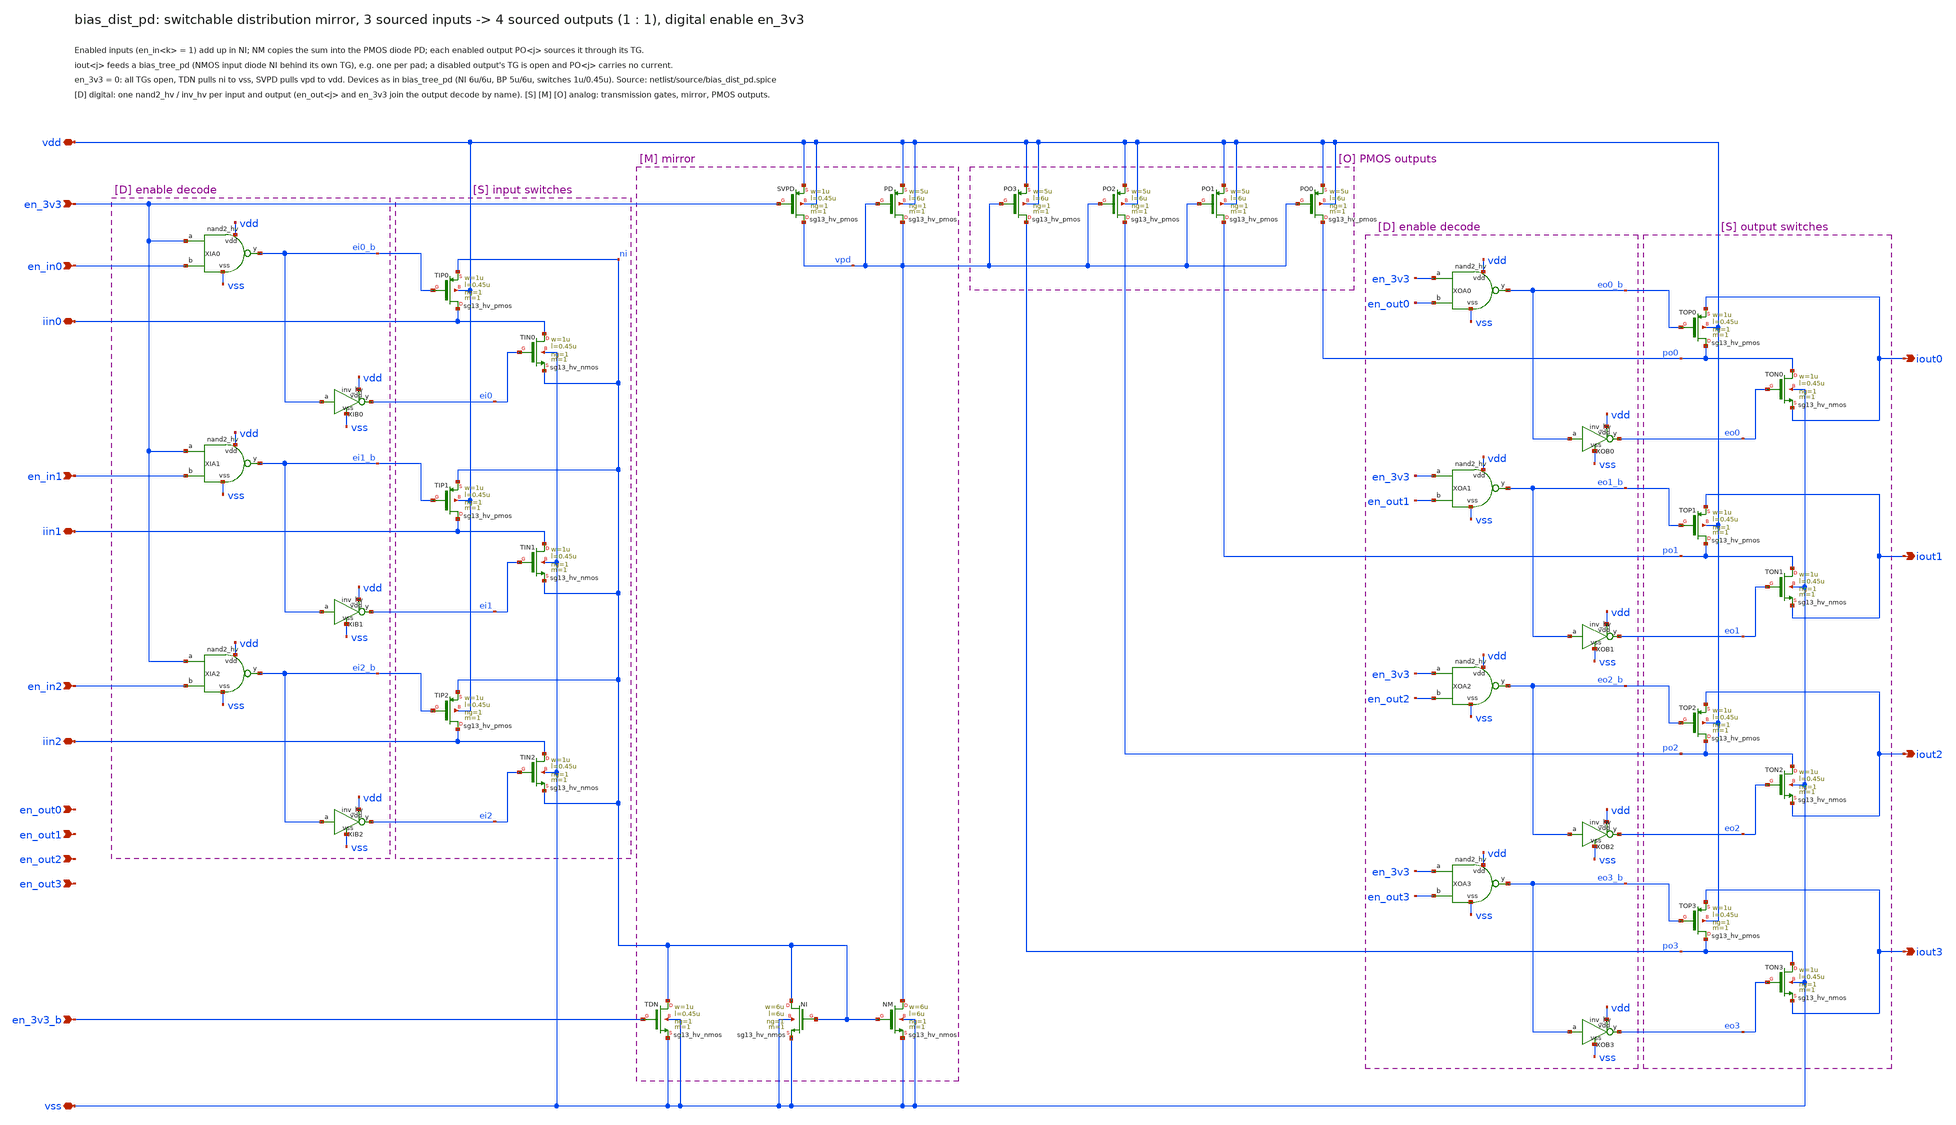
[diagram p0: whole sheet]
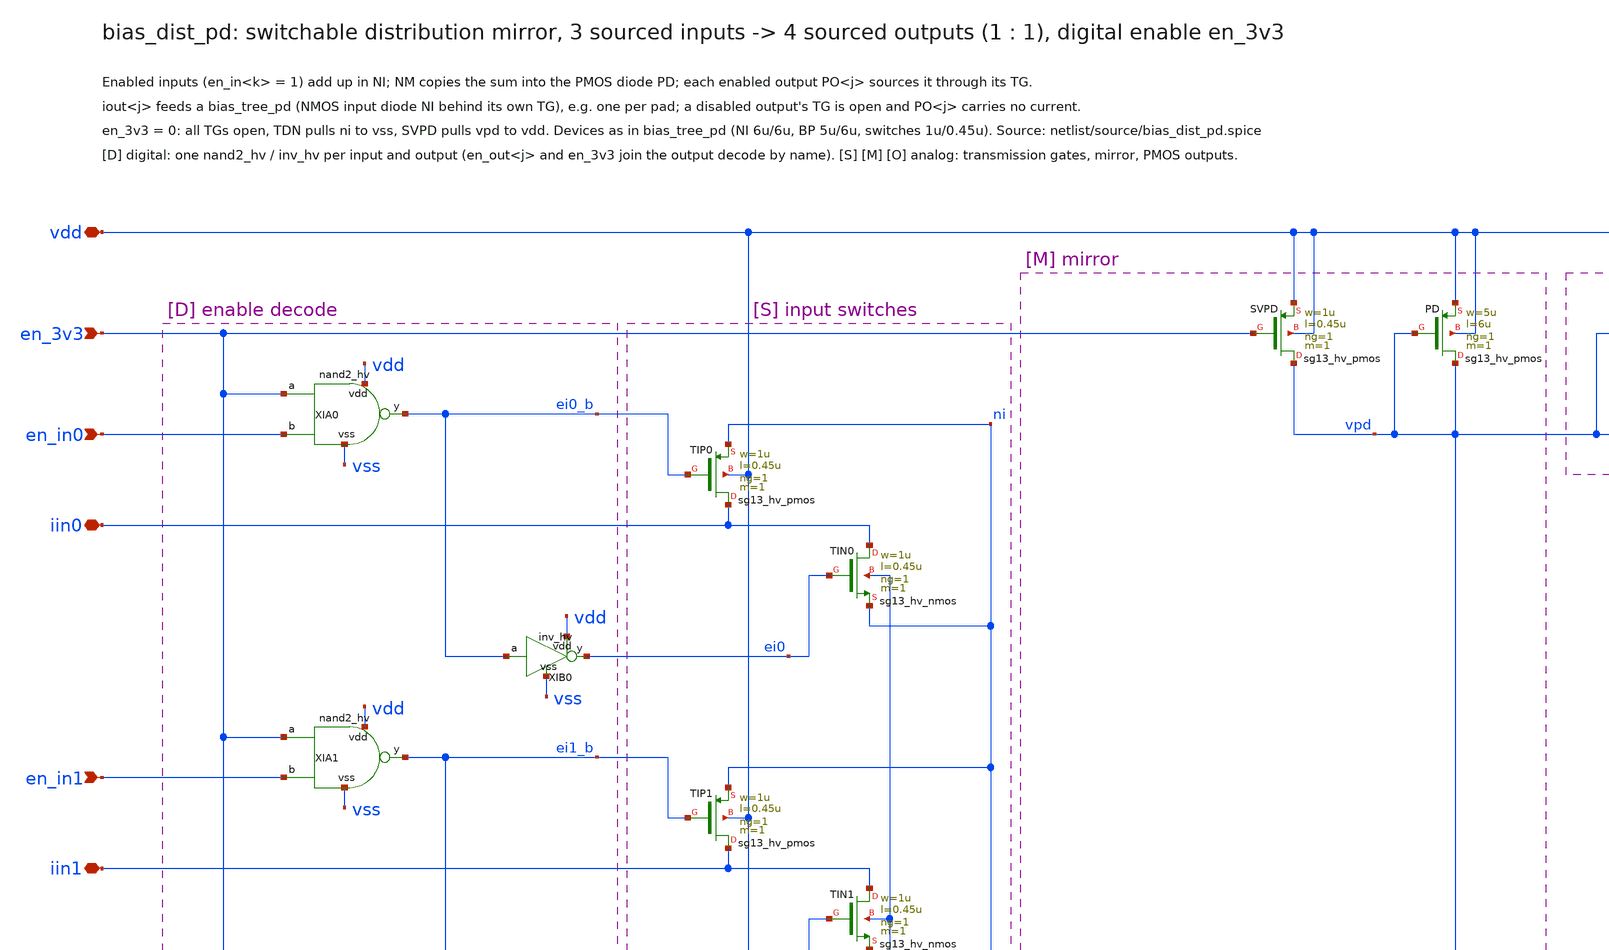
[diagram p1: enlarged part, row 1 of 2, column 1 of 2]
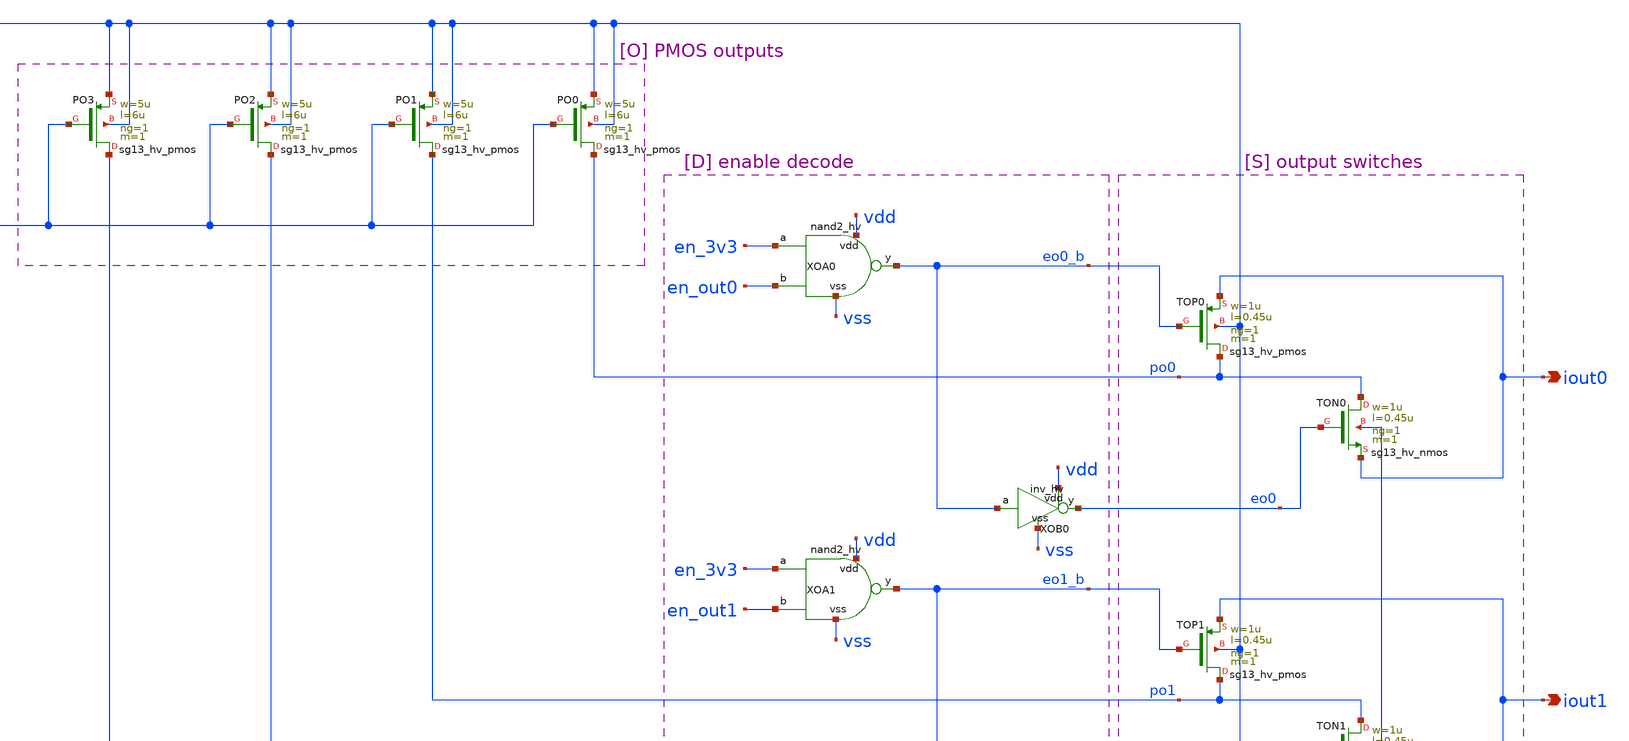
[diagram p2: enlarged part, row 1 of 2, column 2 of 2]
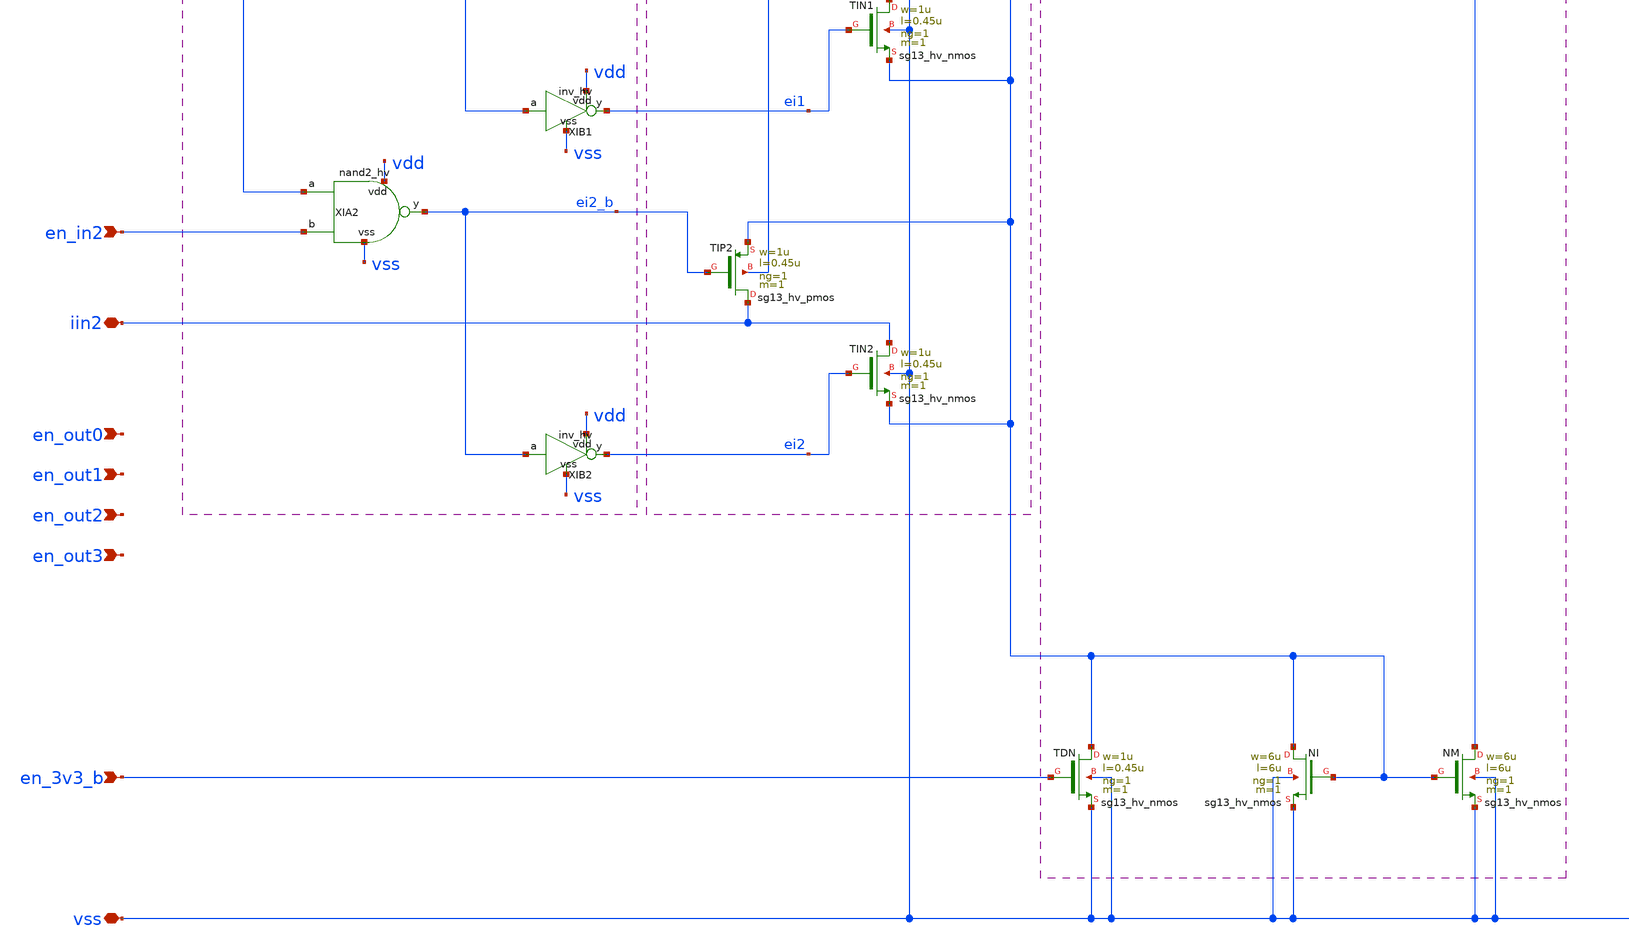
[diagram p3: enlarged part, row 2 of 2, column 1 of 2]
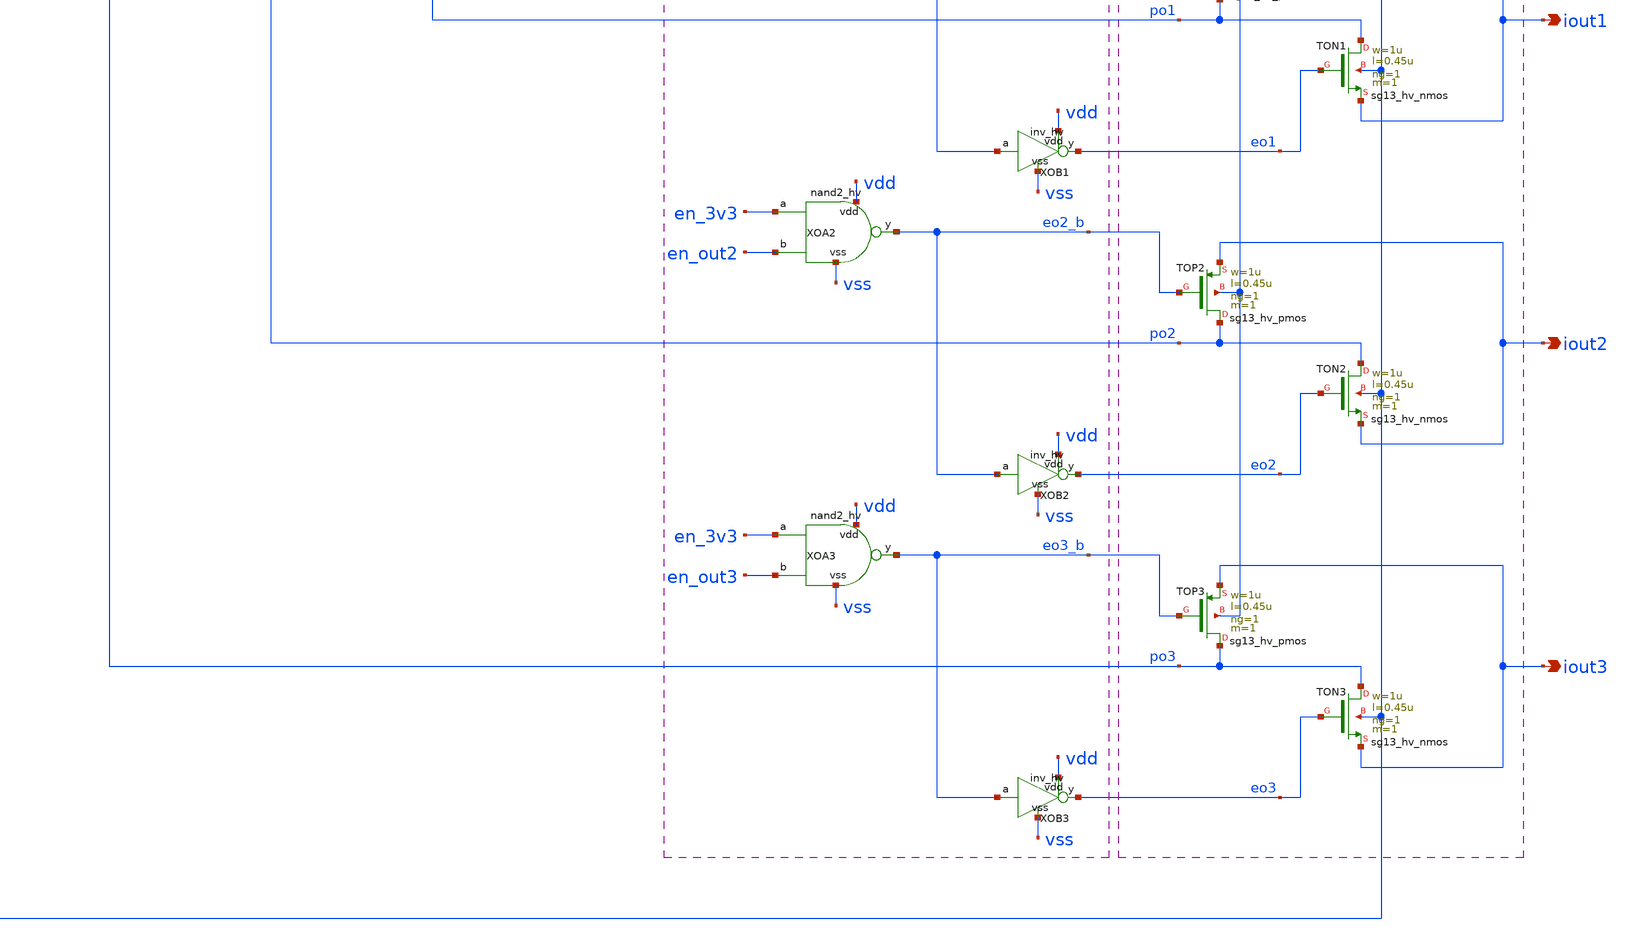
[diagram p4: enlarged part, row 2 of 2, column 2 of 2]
** sch_path: macros/bias_dist_pd/schematic/xschem/bias_dist_pd.sch
**.subckt bias_dist_pd vdd vss en_3v3 en_3v3_b iin0 iin1 iin2 en_in0 en_in1 en_in2 iout0 iout1 iout2
*+ iout3 en_out0 en_out1 en_out2 en_out3
*.iopin vdd
*.iopin vss
*.ipin en_3v3
*.ipin en_3v3_b
*.iopin iin0
*.iopin iin1
*.iopin iin2
*.ipin en_in0
*.ipin en_in1
*.ipin en_in2
*.opin iout0
*.opin iout1
*.opin iout2
*.opin iout3
*.ipin en_out0
*.ipin en_out1
*.ipin en_out2
*.ipin en_out3
XTIN0 iin0 ei0 ni vss sg13_hv_nmos w=1u l=0.45u ng=1 m=1 mm_ok=1
XTIP0 iin0 ei0_b ni vdd sg13_hv_pmos w=1u l=0.45u ng=1 m=1 mm_ok=1
XTIN1 iin1 ei1 ni vss sg13_hv_nmos w=1u l=0.45u ng=1 m=1 mm_ok=1
XTIP1 iin1 ei1_b ni vdd sg13_hv_pmos w=1u l=0.45u ng=1 m=1 mm_ok=1
XTIN2 iin2 ei2 ni vss sg13_hv_nmos w=1u l=0.45u ng=1 m=1 mm_ok=1
XTIP2 iin2 ei2_b ni vdd sg13_hv_pmos w=1u l=0.45u ng=1 m=1 mm_ok=1
XTDN ni en_3v3_b vss vss sg13_hv_nmos w=1u l=0.45u ng=1 m=1 mm_ok=1
XNI ni ni vss vss sg13_hv_nmos w=6u l=6u ng=1 m=1 mm_ok=1
XNM vpd ni vss vss sg13_hv_nmos w=6u l=6u ng=1 m=1 mm_ok=1
XPD vpd vpd vdd vdd sg13_hv_pmos w=5u l=6u ng=1 m=1 mm_ok=1
XSVPD vpd en_3v3 vdd vdd sg13_hv_pmos w=1u l=0.45u ng=1 m=1 mm_ok=1
XPO0 po0 vpd vdd vdd sg13_hv_pmos w=5u l=6u ng=1 m=1 mm_ok=1
XTON0 po0 eo0 iout0 vss sg13_hv_nmos w=1u l=0.45u ng=1 m=1 mm_ok=1
XTOP0 po0 eo0_b iout0 vdd sg13_hv_pmos w=1u l=0.45u ng=1 m=1 mm_ok=1
XPO1 po1 vpd vdd vdd sg13_hv_pmos w=5u l=6u ng=1 m=1 mm_ok=1
XTON1 po1 eo1 iout1 vss sg13_hv_nmos w=1u l=0.45u ng=1 m=1 mm_ok=1
XTOP1 po1 eo1_b iout1 vdd sg13_hv_pmos w=1u l=0.45u ng=1 m=1 mm_ok=1
XPO2 po2 vpd vdd vdd sg13_hv_pmos w=5u l=6u ng=1 m=1 mm_ok=1
XTON2 po2 eo2 iout2 vss sg13_hv_nmos w=1u l=0.45u ng=1 m=1 mm_ok=1
XTOP2 po2 eo2_b iout2 vdd sg13_hv_pmos w=1u l=0.45u ng=1 m=1 mm_ok=1
XPO3 po3 vpd vdd vdd sg13_hv_pmos w=5u l=6u ng=1 m=1 mm_ok=1
XTON3 po3 eo3 iout3 vss sg13_hv_nmos w=1u l=0.45u ng=1 m=1 mm_ok=1
XTOP3 po3 eo3_b iout3 vdd sg13_hv_pmos w=1u l=0.45u ng=1 m=1 mm_ok=1
XIA0 vdd vss en_3v3 en_in0 ei0_b nand2_hv
XIB0 vdd vss ei0_b ei0 inv_hv
XIA1 vdd vss en_3v3 en_in1 ei1_b nand2_hv
XIB1 vdd vss ei1_b ei1 inv_hv
XIA2 vdd vss en_3v3 en_in2 ei2_b nand2_hv
XIB2 vdd vss ei2_b ei2 inv_hv
XOA0 vdd vss en_3v3 en_out0 eo0_b nand2_hv
XOB0 vdd vss eo0_b eo0 inv_hv
XOA1 vdd vss en_3v3 en_out1 eo1_b nand2_hv
XOB1 vdd vss eo1_b eo1 inv_hv
XOA2 vdd vss en_3v3 en_out2 eo2_b nand2_hv
XOB2 vdd vss eo2_b eo2 inv_hv
XOA3 vdd vss en_3v3 en_out3 eo3_b nand2_hv
XOB3 vdd vss eo3_b eo3 inv_hv
**.ends

* expanding   symbol:  nand2_hv.sym # of pins=5
** sym_path: macros/hv_logic/schematic/xschem/nand2_hv.sym
** sch_path: macros/hv_logic/schematic/xschem/nand2_hv.sch
.subckt nand2_hv vdd vss a b y
*.iopin vdd
*.iopin vss
*.ipin a
*.ipin b
*.opin y
XPA y a vdd vdd sg13_hv_pmos w=1u l=0.45u ng=1 m=1 mm_ok=1
XPB y b vdd vdd sg13_hv_pmos w=1u l=0.45u ng=1 m=1 mm_ok=1
XNA y a n1 vss sg13_hv_nmos w=1u l=0.45u ng=1 m=1 mm_ok=1
XNB n1 b vss vss sg13_hv_nmos w=1u l=0.45u ng=1 m=1 mm_ok=1
.ends


* expanding   symbol:  inv_hv.sym # of pins=4
** sym_path: macros/hv_logic/schematic/xschem/inv_hv.sym
** sch_path: macros/hv_logic/schematic/xschem/inv_hv.sch
.subckt inv_hv vdd vss a y
*.iopin vdd
*.iopin vss
*.ipin a
*.opin y
XP y a vdd vdd sg13_hv_pmos w=1u l=0.45u ng=1 m=1 mm_ok=1
XN y a vss vss sg13_hv_nmos w=1u l=0.45u ng=1 m=1 mm_ok=1
.ends

.end
